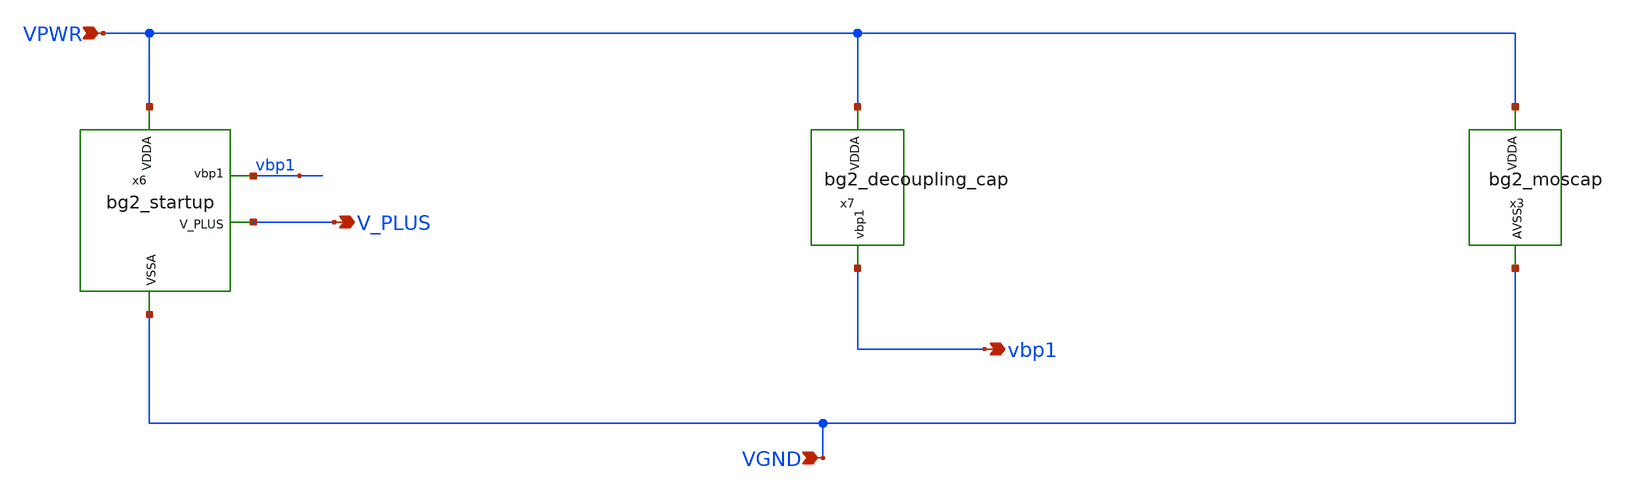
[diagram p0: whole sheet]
** sch_path: lef/lef/gds/bg2_top_tt_v3.sch
**.subckt bg2_top_tt_v3 VGND VPWR vbp1 V_PLUS
*.ipin VGND
*.ipin VPWR
*.opin vbp1
*.opin V_PLUS
x3 VPWR VGND bg2_moscap
x7 VPWR vbp1 bg2_decoupling_cap
x6 VPWR vbp1 V_PLUS VGND bg2_startup
**.ends
.end
